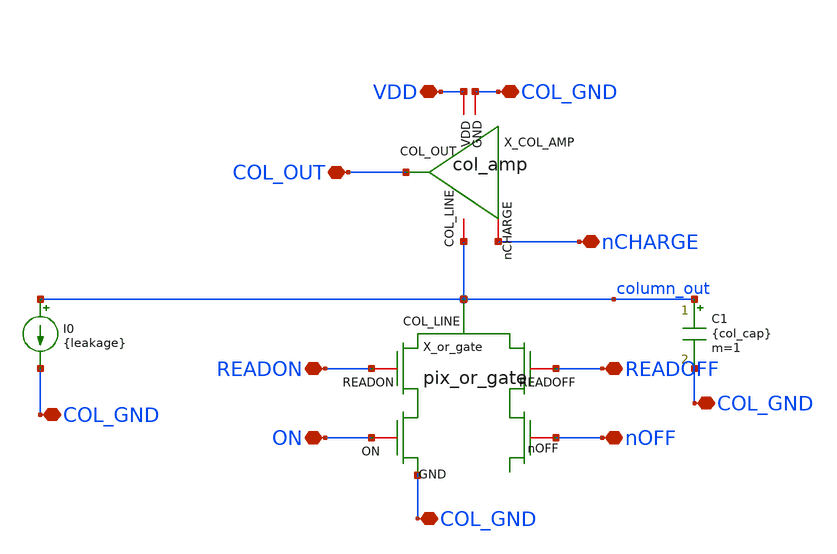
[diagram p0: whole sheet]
** sch_path: analog/xschem/col_amp_v2_std_vds/xschem/TRAN_TR_TB.sch
**.subckt TRAN_TR_TB nCHARGE nOFF READOFF ON READON COL_GND COL_GND COL_GND VDD COL_OUT COL_GND
*.iopin nCHARGE
*.iopin nOFF
*.iopin READOFF
*.iopin ON
*.iopin READON
*.iopin COL_GND
*.iopin COL_GND
*.iopin COL_GND
*.iopin VDD
*.iopin COL_OUT
*.iopin COL_GND
X_COL_AMP VDD nCHARGE COL_OUT COL_GND column_out col_amp
C1 column_out COL_GND {col_cap} m=1
X_or_gate column_out READOFF READON nOFF ON COL_GND pix_or_gate
I0 column_out COL_GND {leakage}
**.ends
**** begin user architecture code


.lib /home/alienfalcon/.ciel/sky130B/libs.tech/combined/sky130.lib.spice tt_mm

.param vdd = 1.8
.param tr = 1p
.param tf = 1p
.param pw = 1u
.param col_cap = 300f
.param leakage = 5p

.option trtol=1 abstol=1p chgtol=4e-16 vntol=1e-6 reltol=1e-6
.option temp = 27

.save v(COL_OUT) tset_col tr_col_out nosub nointernals

V_VDD VDD COL_GND DC {vdd}
V_GND COL_GND 0 DC 0
V_ON ON COL_GND DC {vdd}
V_nOFF nOFF COL_GND DC 0
V_READON READON COL_GND pulse(0 {vdd} {3*pw} {tr} {tf} {pw} {5*pw})
V_READOFF READOFF COL_GND DC 0
V_nCHARGE nCHARGE COL_GND pulse({vdd} 0 {pw} {tr} {tf} {pw} {5*pw})

.control
	option SEED=random
	let mc_runs = 3
	let run = 1
	let V_diff = 0
	let Vc_10 = 0
	let Vc_90 = 0
	let Vc_set_low = 0
	let Vc_set_high = 0
	let start_pulse = 1u
	let tset_col = 0
	let tset_col_high_trig = 0
	let tset_col_low_trig = 0
	let tr_col_out = 0

	*let rise_time_col_out vector(mc_runs)
	*reshape rise_time_col_out [mc_runs]

	*let settling_time_col_out vector(mc_runs)
	*reshape settling_time_col_out [mc_runs]

	*save v(column_out) v(nCHARGE) v(COL_OUT) v(ON) v(nOFF) v(READON) v(READOFF) tset_col tr_col_out
+ nosub nointernals
	save none

	op
	write TRAN_TR_TB.raw

	set appendwrite
	dowhile run <= mc_runs

		*save v(COL_OUT) rise_time_col_out settling_time_col_out nosub nointernals
		save v(COL_OUT) tset_col tr_col_out nosub nointernals
		optran 0 0 0 1p 10n 0
		tran 0.1n 2u

		set run = $&run

		meas tran Vc_max FIND v(COL_OUT) AT=1.3u
		meas tran Vc_min FIND v(COL_OUT) AT=0.3u
		let V_diff = Vc_max - Vc_min
		let Vc_10 = V_diff*0.1 + Vc_min
		let Vc_90 = V_diff*0.9 + Vc_min
		let Vc_set_low = Vc_max*0.98
		let Vc_set_high = Vc_max*1.02

		meas tran tr_col_out TRIG v(COL_OUT) VAL=Vc_10 CROSS=1 TARG v(COL_OUT) VAL=Vc_90 CROSS=1
		*meas tran tf_col_out TRIG v(COL_OUT) VAL=Vc_90 CROSS=2 TARG v(COL_OUT) VAL=Vc_10 CROSS=2
		meas tran tset_col_low_trig WHEN v(COL_OUT)=Vc_set_low RISE=LAST

		let tset_col_high_trig = tset_col_low_trig
		meas tran tset_col_high_trig WHEN v(COL_OUT)=Vc_set_high FALL=LAST

		let tset_col = ((tset_col_low_trig + tset_col_high_trig)/2) - start_pulse

		write TRAN_TR_TB.raw tset_col tr_col_out
		let run = run + 1
		reset

	end
	unset appendwrite




.endc




**** end user architecture code
.end
